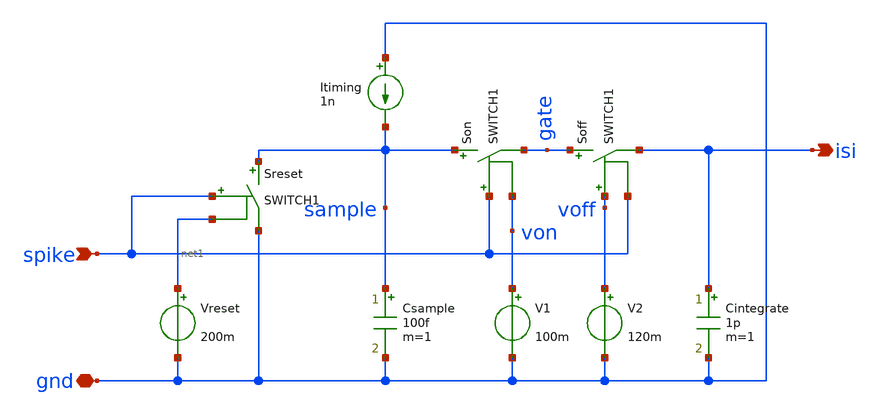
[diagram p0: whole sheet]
** sch_path: playground/InterServicesIntelligence.sch
**.subckt InterServicesIntelligence gnd spike isi
*.iopin gnd
*.ipin spike
*.opin isi
Csample sample gnd 100f m=1
Itiming gnd sample 1n
Son sample gate spike von SWITCH1
Sreset sample gnd spike net1 SWITCH1
Cintegrate isi gnd 1p m=1
V1 von gnd 100m
Vreset net1 gnd 200m
Soff gate isi voff spike SWITCH1
V2 voff gnd 120m
**.ends
.end
